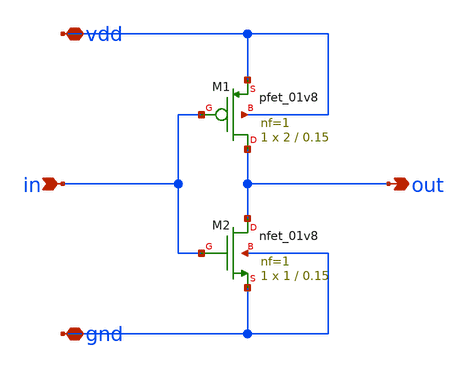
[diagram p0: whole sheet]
** sch_path: examples/analog/my_inverter.sch
**.subckt my_inverter in out vdd gnd
*.ipin in
*.opin out
*.iopin vdd
*.iopin gnd
XM1 out in vdd vdd sky130_fd_pr__pfet_01v8 L=0.15 W=2 nf=1 ad='int((nf+1)/2) * W/nf * 0.29' as='int((nf+2)/2) * W/nf * 0.29'
+ pd='2*int((nf+1)/2) * (W/nf + 0.29)' ps='2*int((nf+2)/2) * (W/nf + 0.29)' nrd='0.29 / W' nrs='0.29 / W'
+ sa=0 sb=0 sd=0 mult=1 m=1
XM2 out in gnd gnd sky130_fd_pr__nfet_01v8 L=0.15 W=1 nf=1 ad='int((1 + 1)/2) * 1 / 1 * 0.29' as='int((1 + 2)/2) * 1 / 1 * 0.29'
+ pd='2*int((1 + 1)/2) * (1 / 1 + 0.29)' ps='2*int((1 + 2)/2) * (1 / 1 + 0.29)' nrd='0.29 / 1 ' nrs='0.29 / 1 '
+ sa=0 sb=0 sd=0 mult=1 m=1
**.ends
.end
